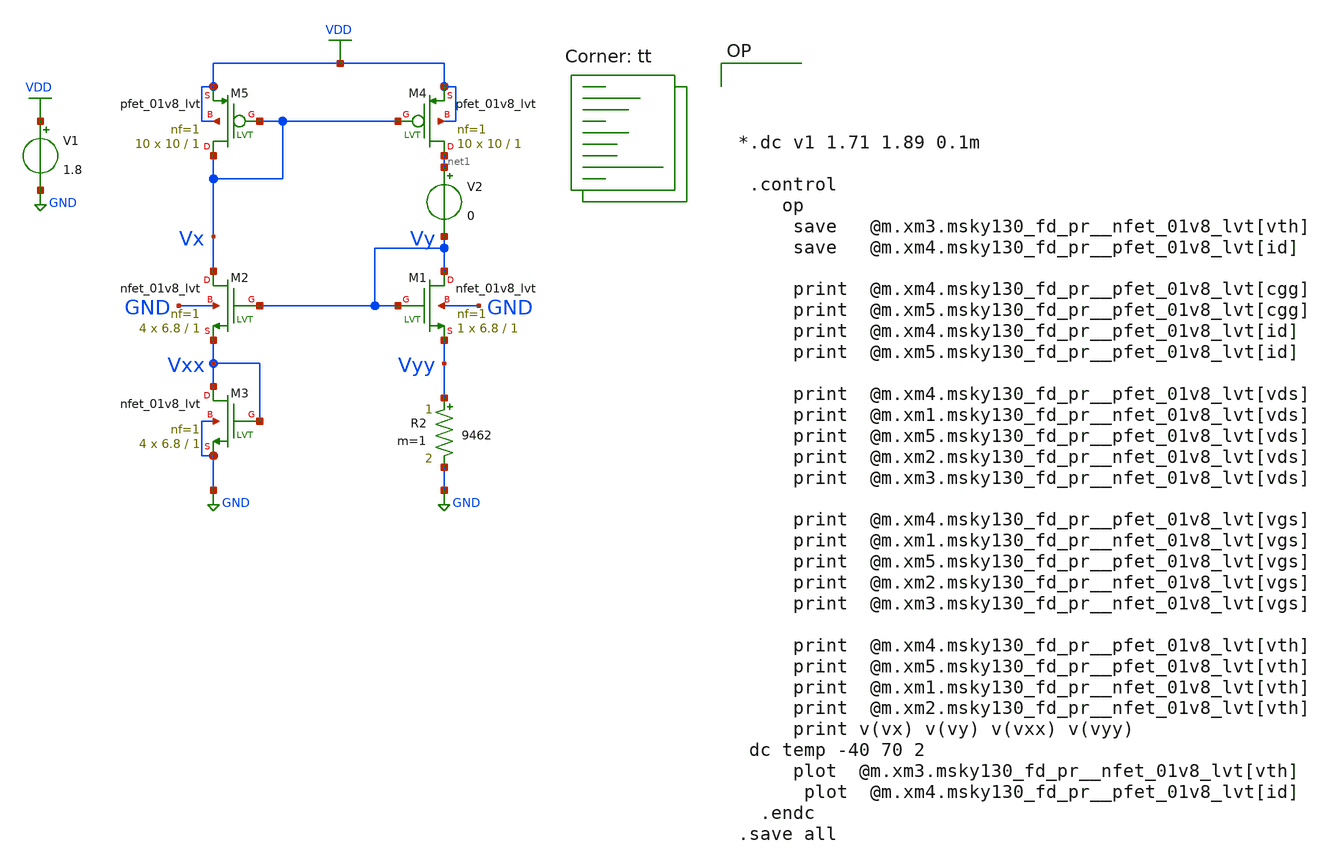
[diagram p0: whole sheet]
** sch_path: pll/lc_vco_lib/Hossam_Tarek/Biasing Circuits/xschem/constant GM0.sch
**.subckt constant GM0
XM1 Vy Vy Vyy GND sky130_fd_pr__nfet_01v8_lvt L=1 W=6.8 nf=1 ad='int((nf+1)/2) * W/nf * 0.29' as='int((nf+2)/2) * W/nf * 0.29'
+ pd='2*int((nf+1)/2) * (W/nf + 0.29)' ps='2*int((nf+2)/2) * (W/nf + 0.29)' nrd='0.29 / W' nrs='0.29 / W'
+ sa=0 sb=0 sd=0 mult=1 m=1
XM2 Vx Vy Vxx GND sky130_fd_pr__nfet_01v8_lvt L=1 W=6.8 nf=1 ad='int((nf+1)/2) * W/nf * 0.29' as='int((nf+2)/2) * W/nf * 0.29'
+ pd='2*int((nf+1)/2) * (W/nf + 0.29)' ps='2*int((nf+2)/2) * (W/nf + 0.29)' nrd='0.29 / W' nrs='0.29 / W'
+ sa=0 sb=0 sd=0 mult=4 m=4
XM3 Vxx Vxx GND GND sky130_fd_pr__nfet_01v8_lvt L=1 W=6.8 nf=1 ad='int((nf+1)/2) * W/nf * 0.29' as='int((nf+2)/2) * W/nf * 0.29'
+ pd='2*int((nf+1)/2) * (W/nf + 0.29)' ps='2*int((nf+2)/2) * (W/nf + 0.29)' nrd='0.29 / W' nrs='0.29 / W'
+ sa=0 sb=0 sd=0 mult=4 m=4
XM4 net1 Vx VDD VDD sky130_fd_pr__pfet_01v8_lvt L=1 W=10 nf=1 ad='int((nf+1)/2) * W/nf * 0.29' as='int((nf+2)/2) * W/nf * 0.29'
+ pd='2*int((nf+1)/2) * (W/nf + 0.29)' ps='2*int((nf+2)/2) * (W/nf + 0.29)' nrd='0.29 / W' nrs='0.29 / W'
+ sa=0 sb=0 sd=0 mult=10 m=10
XM5 Vx Vx VDD VDD sky130_fd_pr__pfet_01v8_lvt L=1 W=10 nf=1 ad='int((nf+1)/2) * W/nf * 0.29' as='int((nf+2)/2) * W/nf * 0.29'
+ pd='2*int((nf+1)/2) * (W/nf + 0.29)' ps='2*int((nf+2)/2) * (W/nf + 0.29)' nrd='0.29 / W' nrs='0.29 / W'
+ sa=0 sb=0 sd=0 mult=10 m=10
V1 VDD GND 1.8
R2 Vyy GND 9462 m=1
V2 net1 Vy 0
**** begin user architecture code




*.dc v1 1.71 1.89 0.1m

 .control
    op
     save   @m.xm3.msky130_fd_pr__nfet_01v8_lvt[vth]
     save   @m.xm4.msky130_fd_pr__pfet_01v8_lvt[id]

     print  @m.xm4.msky130_fd_pr__pfet_01v8_lvt[cgg]
     print  @m.xm5.msky130_fd_pr__pfet_01v8_lvt[cgg]
     print  @m.xm4.msky130_fd_pr__pfet_01v8_lvt[id]
     print  @m.xm5.msky130_fd_pr__pfet_01v8_lvt[id]

     print  @m.xm4.msky130_fd_pr__pfet_01v8_lvt[vds]
     print  @m.xm1.msky130_fd_pr__nfet_01v8_lvt[vds]
     print  @m.xm5.msky130_fd_pr__pfet_01v8_lvt[vds]
     print  @m.xm2.msky130_fd_pr__nfet_01v8_lvt[vds]
     print  @m.xm3.msky130_fd_pr__nfet_01v8_lvt[vds]

     print  @m.xm4.msky130_fd_pr__pfet_01v8_lvt[vgs]
     print  @m.xm1.msky130_fd_pr__nfet_01v8_lvt[vgs]
     print  @m.xm5.msky130_fd_pr__pfet_01v8_lvt[vgs]
     print  @m.xm2.msky130_fd_pr__nfet_01v8_lvt[vgs]
     print  @m.xm3.msky130_fd_pr__nfet_01v8_lvt[vgs]

     print  @m.xm4.msky130_fd_pr__pfet_01v8_lvt[vth]
     print  @m.xm5.msky130_fd_pr__pfet_01v8_lvt[vth]
     print  @m.xm1.msky130_fd_pr__nfet_01v8_lvt[vth]
     print  @m.xm2.msky130_fd_pr__nfet_01v8_lvt[vth]
     print v(vx) v(vy) v(vxx) v(vyy)
 dc temp -40 70 2
     plot  @m.xm3.msky130_fd_pr__nfet_01v8_lvt[vth]
      plot  @m.xm4.msky130_fd_pr__pfet_01v8_lvt[id]
  .endc
.save all

.lib $::SKYWATER_MODELS/sky130.lib.spice tt
**** end user architecture code
**.ends
.GLOBAL GND
.GLOBAL VDD
.end
